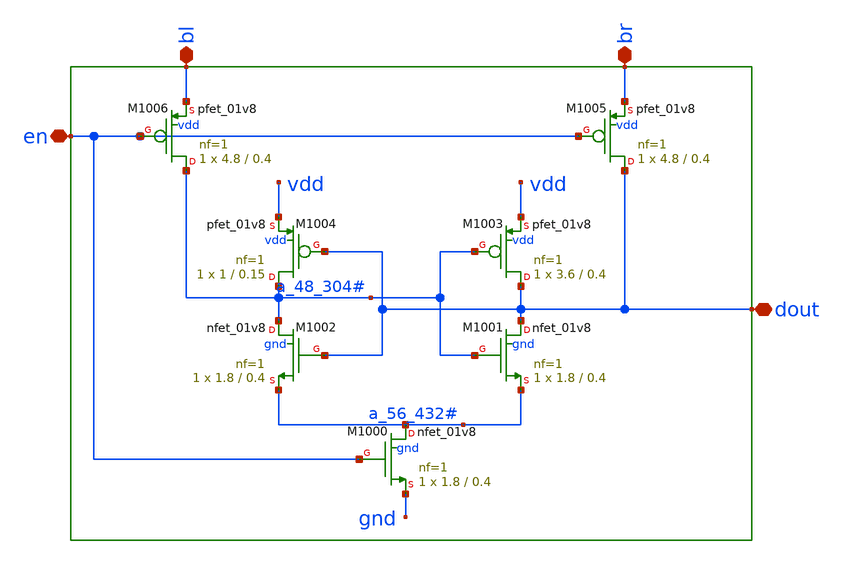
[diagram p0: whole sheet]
** sch_path: sram_4_16_scn4m/sense_amp.sch
**.subckt sense_amp bl br dout en
*.iopin bl
*.iopin br
*.iopin dout
*.iopin en
XM1004 a_48_304# dout vdd vdd sky130_fd_pr__pfet_01v8 L=0.15 W=1 nf=1 ad='int((nf+1)/2) * W/nf * 0.29'
+ as='int((nf+2)/2) * W/nf * 0.29' pd='2*int((nf+1)/2) * (W/nf + 0.29)' ps='2*int((nf+2)/2) * (W/nf + 0.29)'
+ nrd='0.29 / W' nrs='0.29 / W' sa=0 sb=0 sd=0 mult=1 m=1
XM1003 dout a_48_304# vdd vdd sky130_fd_pr__pfet_01v8 L=0.4 W=3.6 nf=1 ad='int((nf+1)/2) * W/nf * 0.29'
+ as='int((nf+2)/2) * W/nf * 0.29' pd='2*int((nf+1)/2) * (W/nf + 0.29)' ps='2*int((nf+2)/2) * (W/nf + 0.29)'
+ nrd='0.29 / W' nrs='0.29 / W' sa=0 sb=0 sd=0 mult=1 m=1
XM1002 a_48_304# dout a_56_432# gnd sky130_fd_pr__nfet_01v8 L=0.4 W=1.8 nf=1 ad='int((nf+1)/2) * W/nf * 0.29'
+ as='int((nf+2)/2) * W/nf * 0.29' pd='2*int((nf+1)/2) * (W/nf + 0.29)' ps='2*int((nf+2)/2) * (W/nf + 0.29)'
+ nrd='0.29 / W' nrs='0.29 / W' sa=0 sb=0 sd=0 mult=1 m=1
XM1001 dout a_48_304# a_56_432# gnd sky130_fd_pr__nfet_01v8 L=0.4 W=1.8 nf=1 ad='int((nf+1)/2) * W/nf * 0.29'
+ as='int((nf+2)/2) * W/nf * 0.29' pd='2*int((nf+1)/2) * (W/nf + 0.29)' ps='2*int((nf+2)/2) * (W/nf + 0.29)'
+ nrd='0.29 / W' nrs='0.29 / W' sa=0 sb=0 sd=0 mult=1 m=1
XM1000 a_56_432# en gnd gnd sky130_fd_pr__nfet_01v8 L=0.4 W=1.8 nf=1 ad='int((nf+1)/2) * W/nf * 0.29'
+ as='int((nf+2)/2) * W/nf * 0.29' pd='2*int((nf+1)/2) * (W/nf + 0.29)' ps='2*int((nf+2)/2) * (W/nf + 0.29)'
+ nrd='0.29 / W' nrs='0.29 / W' sa=0 sb=0 sd=0 mult=1 m=1
XM1006 a_48_304# en bl vdd sky130_fd_pr__pfet_01v8 L=0.4 W=4.8 nf=1 ad='int((nf+1)/2) * W/nf * 0.29'
+ as='int((nf+2)/2) * W/nf * 0.29' pd='2*int((nf+1)/2) * (W/nf + 0.29)' ps='2*int((nf+2)/2) * (W/nf + 0.29)'
+ nrd='0.29 / W' nrs='0.29 / W' sa=0 sb=0 sd=0 mult=1 m=1
XM1005 dout en br vdd sky130_fd_pr__pfet_01v8 L=0.4 W=4.8 nf=1 ad='int((nf+1)/2) * W/nf * 0.29' as='int((nf+2)/2) * W/nf * 0.29'
+ pd='2*int((nf+1)/2) * (W/nf + 0.29)' ps='2*int((nf+2)/2) * (W/nf + 0.29)' nrd='0.29 / W' nrs='0.29 / W'
+ sa=0 sb=0 sd=0 mult=1 m=1
**.ends
.end
